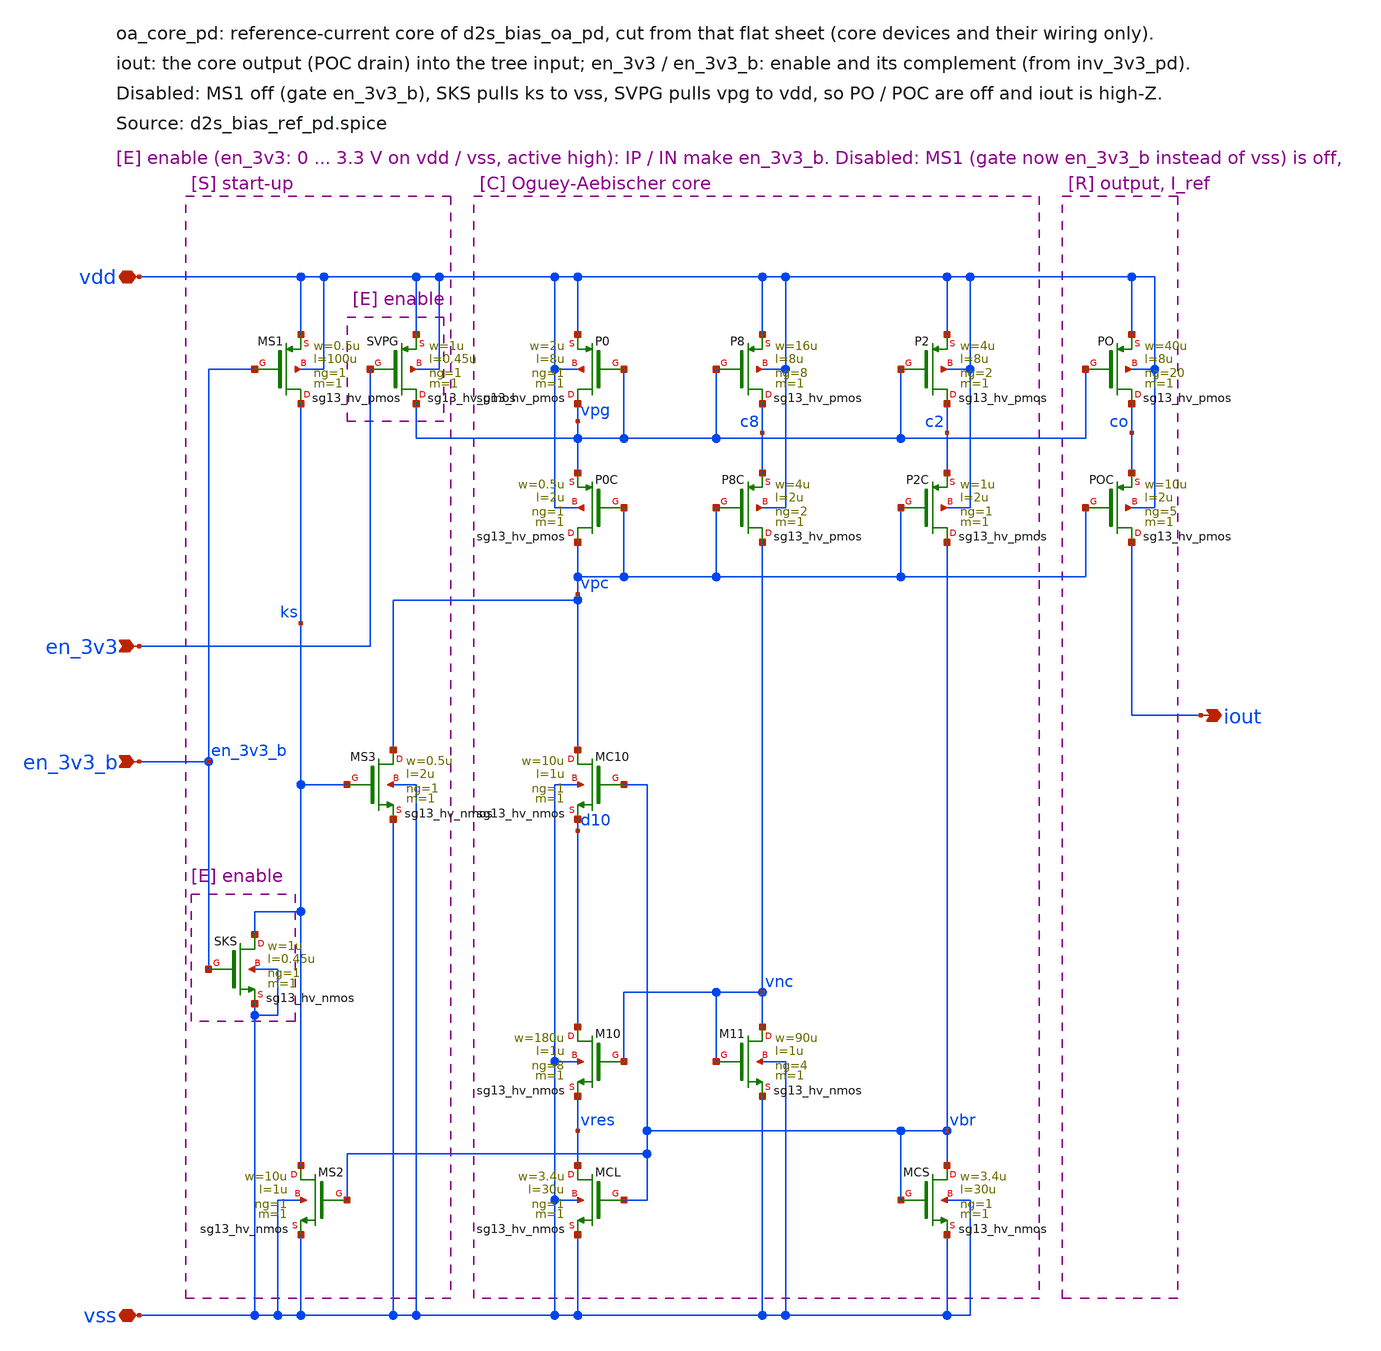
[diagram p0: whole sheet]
** sch_path: sudelbuecher/design_considerations/consolidation/bias_hierarchy_2026-10-27/before/macros/d2s_bias_sel_pd/schematic/xschem/oa_core_pd.sch
**.subckt oa_core_pd vdd vss en_3v3 en_3v3_b iout
*.iopin vdd
*.iopin vss
*.ipin en_3v3
*.ipin en_3v3_b
*.opin iout
XMS1 ks en_3v3_b vdd vdd sg13_hv_pmos w=0.5u l=100u ng=1 m=1 mm_ok=1
XMS2 ks vbr vss vss sg13_hv_nmos w=10u l=1u ng=1 m=1 mm_ok=1
XMS3 vpc ks vss vss sg13_hv_nmos w=0.5u l=2u ng=1 m=1 mm_ok=1
XP0 vpg vpg vdd vdd sg13_hv_pmos w=2u l=8u ng=1 m=1 mm_ok=1
XP0C vpc vpc vpg vdd sg13_hv_pmos w=0.5u l=2u ng=1 m=1 mm_ok=1
XMC10 vpc vbr d10 vss sg13_hv_nmos w=10u l=1u ng=1 m=1 mm_ok=1
XM10 d10 vnc vres vss sg13_hv_nmos w=180u l=1u ng=8 m=1 mm_ok=1
XMCL vres vbr vss vss sg13_hv_nmos w=3.4u l=30u ng=1 m=1 mm_ok=1
XP8 c8 vpg vdd vdd sg13_hv_pmos w=16u l=8u ng=8 m=1 mm_ok=1
XP8C vnc vpc c8 vdd sg13_hv_pmos w=4u l=2u ng=2 m=1 mm_ok=1
XM11 vnc vnc vss vss sg13_hv_nmos w=90u l=1u ng=4 m=1 mm_ok=1
XP2 c2 vpg vdd vdd sg13_hv_pmos w=4u l=8u ng=2 m=1 mm_ok=1
XP2C vbr vpc c2 vdd sg13_hv_pmos w=1u l=2u ng=1 m=1 mm_ok=1
XMCS vbr vbr vss vss sg13_hv_nmos w=3.4u l=30u ng=1 m=1 mm_ok=1
XPO co vpg vdd vdd sg13_hv_pmos w=40u l=8u ng=20 m=1 mm_ok=1
XPOC iout vpc co vdd sg13_hv_pmos w=10u l=2u ng=5 m=1 mm_ok=1
XSKS ks en_3v3_b vss vss sg13_hv_nmos w=1u l=0.45u ng=1 m=1 mm_ok=1
XSVPG vpg en_3v3 vdd vdd sg13_hv_pmos w=1u l=0.45u ng=1 m=1 mm_ok=1
**.ends
.end
